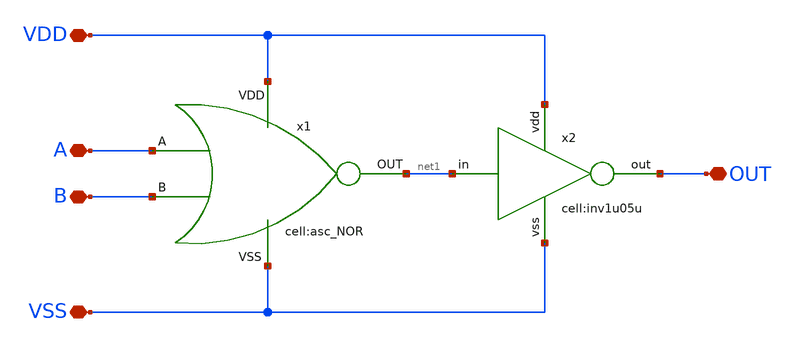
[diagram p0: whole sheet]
** sch_path: designs/libs/core_analog/asc_OR/asc_OR.sch
**.subckt asc_OR VDD A B VSS OUT
*.iopin VDD
*.iopin A
*.iopin B
*.iopin VSS
*.iopin OUT
x1 VDD VSS net1 A B asc_NOR
x2 net1 VDD OUT VSS inv1u05u
**.ends
.end
